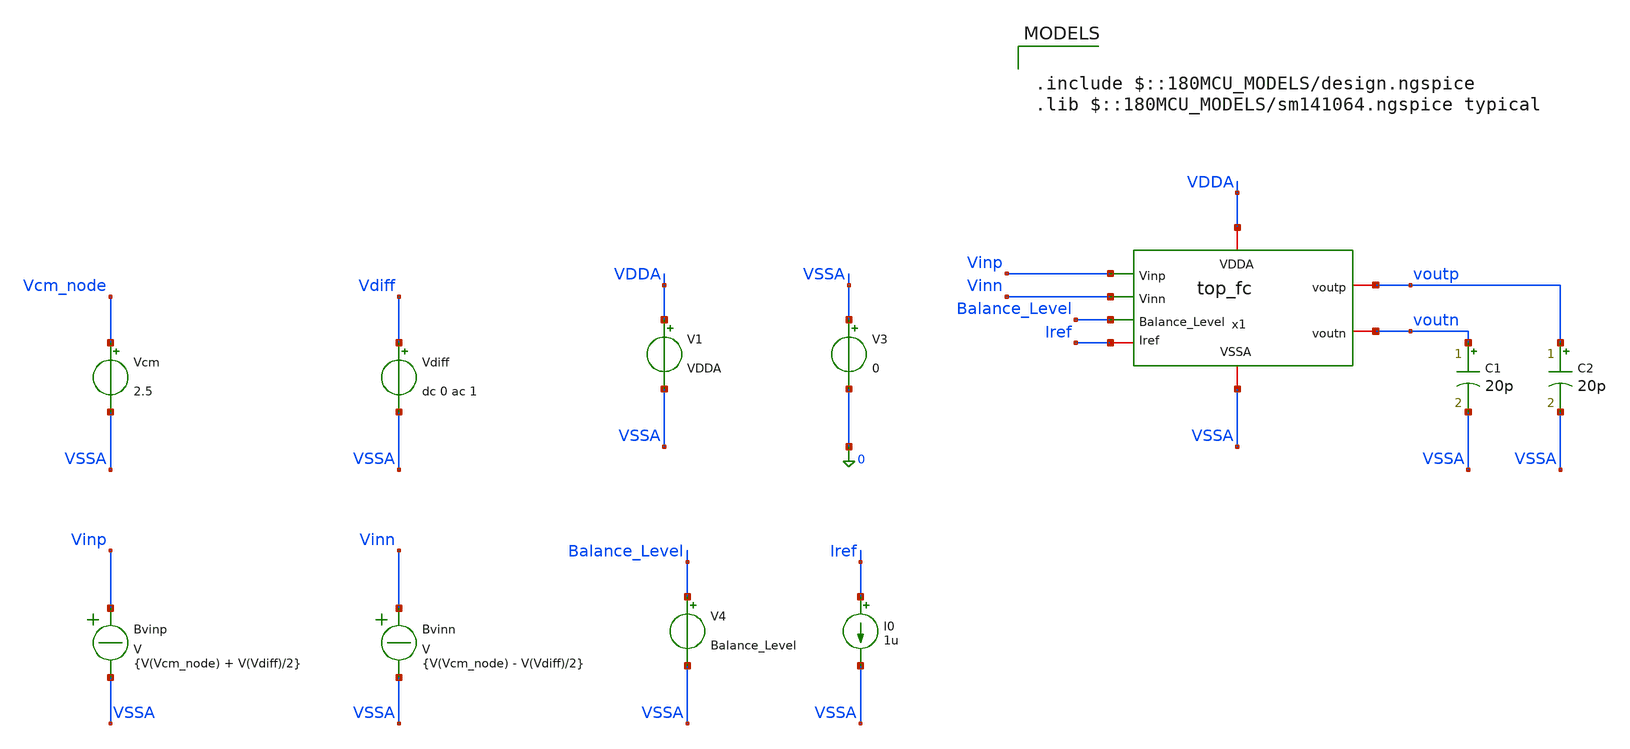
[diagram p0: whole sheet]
** sch_path: Folded_cascode/testbenches/top_fc_icmr_tb.sch
**.subckt top_fc_icmr_tb
x1 Balance_Level Vinp voutp VDDA voutn Vinn Iref VSSA top_fc
C1 voutn VSSA 20p m=1
C2 voutp VSSA 20p m=1
V1 VDDA VSSA VDDA
V3 VSSA 0 0
V4 Balance_Level VSSA Balance_Level
I0 Iref VSSA 1u
Bvinp Vinp VSSA V = {V(Vcm_node) + V(Vdiff)/2}
Bvinn Vinn VSSA V = {V(Vcm_node) - V(Vdiff)/2}
Vcm Vcm_node VSSA 2.5
Vdiff Vdiff VSSA dc 0 ac 1
**** begin user architecture code

.include $::180MCU_MODELS/design.ngspice
.lib $::180MCU_MODELS/sm141064.ngspice typical



.temp 27
.param VDDA = 5
.param Balance_Level = 1.5

.param sw_stat_global=0
.param sw_stat_mismatch=0

.control
option sparse
set filetype=ascii
set wr_singlescale
set wr_vecnames
save all
save @m.x1.x1.xm1.m0[id]
save @m.x1.x1.xm1.m0[gm]
save @m.x1.x1.xm1.m0[vgs]
save @m.x1.x1.xm1.m0[vds]
save @m.x1.x1.xm1.m0[vth]
save @m.x1.x1.xm1.m0[gds]
save @m.x1.x1.xm1.m0[vdsat]

save @m.x1.x1.xm2.m0[id]
save @m.x1.x1.xm2.m0[gm]
save @m.x1.x1.xm2.m0[vgs]
save @m.x1.x1.xm2.m0[vds]
save @m.x1.x1.xm2.m0[vth]
save @m.x1.x1.xm2.m0[gds]
save @m.x1.x1.xm2.m0[vdsat]

save @m.x1.x1.xm9.m0[id]
save @m.x1.x1.xm9.m0[gm]
save @m.x1.x1.xm9.m0[vgs]
save @m.x1.x1.xm9.m0[vds]
save @m.x1.x1.xm9.m0[vth]
save @m.x1.x1.xm9.m0[gds]
save @m.x1.x1.xm9.m0[vdsat]

save @m.x1.x1.xm8.m0[id]
save @m.x1.x1.xm8.m0[gm]
save @m.x1.x1.xm8.m0[vgs]
save @m.x1.x1.xm8.m0[vds]
save @m.x1.x1.xm8.m0[vth]
save @m.x1.x1.xm8.m0[gds]
save @m.x1.x1.xm8.m0[vdsat]

save @m.x1.x1.xm6.m0[id]
save @m.x1.x1.xm6.m0[gm]
save @m.x1.x1.xm6.m0[vgs]
save @m.x1.x1.xm6.m0[vds]
save @m.x1.x1.xm6.m0[vth]
save @m.x1.x1.xm6.m0[gds]
save @m.x1.x1.xm6.m0[vdsat]

save @m.x1.x1.xm5.m0[id]
save @m.x1.x1.xm5.m0[gm]
save @m.x1.x1.xm5.m0[vgs]
save @m.x1.x1.xm5.m0[vds]
save @m.x1.x1.xm5.m0[vth]
save @m.x1.x1.xm5.m0[gds]
save @m.x1.x1.xm5.m0[vdsat]

save @m.x1.x2.xm1.m0[id]
save @m.x1.x2.xm1.m0[gm]
save @m.x1.x2.xm1.m0[vgs]
save @m.x1.x2.xm1.m0[vds]
save @m.x1.x2.xm1.m0[vth]
save @m.x1.x2.xm1.m0[gds]

save @m.x1.x2.xm2.m0[id]
save @m.x1.x2.xm2.m0[gm]
save @m.x1.x2.xm2.m0[vgs]
save @m.x1.x2.xm2.m0[vds]
save @m.x1.x2.xm2.m0[vth]
save @m.x1.x2.xm2.m0[gds]

save @m.x1.x2.xm3.m0[id]
save @m.x1.x2.xm3.m0[gm]
save @m.x1.x2.xm3.m0[vgs]
save @m.x1.x2.xm3.m0[vds]
save @m.x1.x2.xm3.m0[vth]
save @m.x1.x2.xm3.m0[gds]

save @m.x1.x2.xm4.m0[id]
save @m.x1.x2.xm4.m0[gm]
save @m.x1.x2.xm4.m0[vgs]
save @m.x1.x2.xm4.m0[vds]
save @m.x1.x2.xm4.m0[vth]
save @m.x1.x2.xm4.m0[gds]

save @m.x1.x2.xm5.m0[id]
save @m.x1.x2.xm5.m0[gm]
save @m.x1.x2.xm5.m0[vgs]
save @m.x1.x2.xm5.m0[vds]
save @m.x1.x2.xm5.m0[vth]
save @m.x1.x2.xm5.m0[gds]

save @m.x1.x2.xm6.m0[id]
save @m.x1.x2.xm6.m0[gm]
save @m.x1.x2.xm6.m0[vgs]
save @m.x1.x2.xm6.m0[vds]
save @m.x1.x2.xm6.m0[vth]
save @m.x1.x2.xm6.m0[gds]

save @m.x1.x2.xm7.m0[id]
save @m.x1.x2.xm7.m0[gm]
save @m.x1.x2.xm7.m0[vgs]
save @m.x1.x2.xm7.m0[vds]
save @m.x1.x2.xm7.m0[vth]
save @m.x1.x2.xm7.m0[gds]

save @m.x1.x2.xm8.m0[id]
save @m.x1.x2.xm8.m0[gm]
save @m.x1.x2.xm8.m0[vgs]
save @m.x1.x2.xm8.m0[vds]
save @m.x1.x2.xm8.m0[vth]
save @m.x1.x2.xm8.m0[gds]

save @m.x1.x2.xm9.m0[id]
save @m.x1.x2.xm9.m0[gm]
save @m.x1.x2.xm9.m0[vgs]
save @m.x1.x2.xm9.m0[vds]
save @m.x1.x2.xm9.m0[vth]
save @m.x1.x2.xm9.m0[gds]

save @m.x1.x3.xm1.m0[id]
save @m.x1.x3.xm1.m0[gm]
save @m.x1.x3.xm1.m0[vgs]
save @m.x1.x3.xm1.m0[vds]
save @m.x1.x3.xm1.m0[vth]
save @m.x1.x3.xm1.m0[gds]

save @m.x1.x3.xm2.m0[id]
save @m.x1.x3.xm2.m0[gm]
save @m.x1.x3.xm2.m0[vgs]
save @m.x1.x3.xm2.m0[vds]
save @m.x1.x3.xm2.m0[vth]
save @m.x1.x3.xm2.m0[gds]

save @m.x1.x3.xm3.m0[id]
save @m.x1.x3.xm3.m0[gm]
save @m.x1.x3.xm3.m0[vgs]
save @m.x1.x3.xm3.m0[vds]
save @m.x1.x3.xm3.m0[vth]
save @m.x1.x3.xm3.m0[gds]

save @m.x1.x3.xm4.m0[id]
save @m.x1.x3.xm4.m0[gm]
save @m.x1.x3.xm4.m0[vgs]
save @m.x1.x3.xm4.m0[vds]
save @m.x1.x3.xm4.m0[vth]
save @m.x1.x3.xm4.m0[gds]

save @m.x1.x3.xm5.m0[id]
save @m.x1.x3.xm5.m0[gm]
save @m.x1.x3.xm5.m0[vgs]
save @m.x1.x3.xm5.m0[vds]
save @m.x1.x3.xm5.m0[vth]
save @m.x1.x3.xm5.m0[gds]

save @m.x1.x3.xm6.m0[id]
save @m.x1.x3.xm6.m0[gm]
save @m.x1.x3.xm6.m0[vgs]
save @m.x1.x3.xm6.m0[vds]
save @m.x1.x3.xm6.m0[vth]
save @m.x1.x3.xm6.m0[gds]

save @m.x1.x3.xm7.m0[id]
save @m.x1.x3.xm7.m0[gm]
save @m.x1.x3.xm7.m0[vgs]
save @m.x1.x3.xm7.m0[vds]
save @m.x1.x3.xm7.m0[vth]
save @m.x1.x3.xm7.m0[gds]

save @m.x1.x3.xm8.m0[id]
save @m.x1.x3.xm8.m0[gm]
save @m.x1.x3.xm8.m0[vgs]
save @m.x1.x3.xm8.m0[vds]
save @m.x1.x3.xm8.m0[vth]
save @m.x1.x3.xm8.m0[gds]

save @m.x1.x3.xm9.m0[id]
save @m.x1.x3.xm9.m0[gm]
save @m.x1.x3.xm9.m0[vgs]
save @m.x1.x3.xm9.m0[vds]
save @m.x1.x3.xm9.m0[vth]
save @m.x1.x3.xm9.m0[gds]

save @m.x1.x3.xm10.m0[id]
save @m.x1.x3.xm10.m0[gm]
save @m.x1.x3.xm10.m0[vgs]
save @m.x1.x3.xm10.m0[vds]
save @m.x1.x3.xm10.m0[vth]
save @m.x1.x3.xm10.m0[gds]

save @m.x1.x3.xm11.m0[id]
save @m.x1.x3.xm11.m0[gm]
save @m.x1.x3.xm11.m0[vgs]
save @m.x1.x3.xm11.m0[vds]
save @m.x1.x3.xm11.m0[vth]
save @m.x1.x3.xm11.m0[gds]

save @m.x1.x3.xm12.m0[id]
save @m.x1.x3.xm12.m0[gm]
save @m.x1.x3.xm12.m0[vgs]
save @m.x1.x3.xm12.m0[vds]
save @m.x1.x3.xm12.m0[vth]
save @m.x1.x3.xm12.m0[gds]

save @m.x1.x3.xm13.m0[id]
save @m.x1.x3.xm13.m0[gm]
save @m.x1.x3.xm13.m0[vgs]
save @m.x1.x3.xm13.m0[vds]
save @m.x1.x3.xm13.m0[vth]
save @m.x1.x3.xm13.m0[gds]

save @m.x1.x3.xm14.m0[id]
save @m.x1.x3.xm14.m0[gm]
save @m.x1.x3.xm14.m0[vgs]
save @m.x1.x3.xm14.m0[vds]
save @m.x1.x3.xm14.m0[vth]
save @m.x1.x3.xm14.m0[gds]

save @m.x1.x3.xm15.m0[id]
save @m.x1.x3.xm15.m0[gm]
save @m.x1.x3.xm15.m0[vgs]
save @m.x1.x3.xm15.m0[vds]
save @m.x1.x3.xm15.m0[vth]
save @m.x1.x3.xm15.m0[gds]

save @m.x1.x3.xm16.m0[id]
save @m.x1.x3.xm16.m0[gm]
save @m.x1.x3.xm16.m0[vgs]
save @m.x1.x3.xm16.m0[vds]
save @m.x1.x3.xm16.m0[vth]
save @m.x1.x3.xm16.m0[gds]

save @m.x1.x3.xm17.m0[id]
save @m.x1.x3.xm17.m0[gm]
save @m.x1.x3.xm17.m0[vgs]
save @m.x1.x3.xm17.m0[vds]
save @m.x1.x3.xm17.m0[vth]
save @m.x1.x3.xm17.m0[gds]

save @m.x1.x3.xm18.m0[id]
save @m.x1.x3.xm18.m0[gm]
save @m.x1.x3.xm18.m0[vgs]
save @m.x1.x3.xm18.m0[vds]
save @m.x1.x3.xm18.m0[vth]
save @m.x1.x3.xm18.m0[gds]

save @m.x1.x3.xm21.m0[id]
save @m.x1.x3.xm21.m0[gm]
save @m.x1.x3.xm21.m0[vgs]
save @m.x1.x3.xm21.m0[vds]
save @m.x1.x3.xm21.m0[vth]
save @m.x1.x3.xm21.m0[gds]

save @m.x1.x3.xm22.m0[id]
save @m.x1.x3.xm22.m0[gm]
save @m.x1.x3.xm22.m0[vgs]
save @m.x1.x3.xm22.m0[vds]
save @m.x1.x3.xm22.m0[vth]
save @m.x1.x3.xm22.m0[gds]

op
write top_fc_op_tb.raw all

* ------------------------------------------------------------
* Nominal operating point at VCM = 2.5 V
* ------------------------------------------------------------

alter @Vcm[dc] = 2.5

* ------------------------------------------------------------
* Persistent sweep variables
*
* Variables are stored in the CONST plot so they survive
* the creation of each new AC plot.
* ------------------------------------------------------------

setplot const

let vcm_val  = 0
let vcm_stop = 5
let vcm_step = 0.01


* ------------------------------------------------------------
* Remove previous result file
* ------------------------------------------------------------

shell rm -f icmr_gain.dat


* ============================================================
* COMMON-MODE SWEEP
* ============================================================

while vcm_val <= vcm_stop

    * --------------------------------------------------------
    * Set current common-mode voltage
    * --------------------------------------------------------

    alter @Vcm[dc] = $&vcm_val


    * --------------------------------------------------------
    * Low-frequency differential gain
    *
    * Only one AC point is required because no MEAS AT
    * interpolation is used.
    * --------------------------------------------------------

    ac lin 1 1 1


    * --------------------------------------------------------
    * Differential output
    * --------------------------------------------------------

    let vod = v(voutp)-v(voutn)


    * --------------------------------------------------------
    * Differential gain
    *
    * Vdiff AC amplitude = 1 V
    * --------------------------------------------------------

    let ad = vod/v(Vdiff)


    * --------------------------------------------------------
    * Differential gain in dB
    * --------------------------------------------------------

    let gain_now = db(ad)


    * --------------------------------------------------------
    * Store:
    *
    * column 1 = VCM [V]
    * column 2 = differential gain [dB]
    * --------------------------------------------------------

    echo $&const.vcm_val $&gain_now >> icmr_gain.dat


    * --------------------------------------------------------
    * Return to persistent variables
    * --------------------------------------------------------

    setplot const


    * --------------------------------------------------------
    * Increment common-mode voltage
    * --------------------------------------------------------

    let vcm_val = vcm_val + vcm_step

end


* ------------------------------------------------------------
* Restore nominal common-mode voltage
* ------------------------------------------------------------

alter @Vcm[dc] = 2.5

.endc


**** end user architecture code
**.ends
.end
